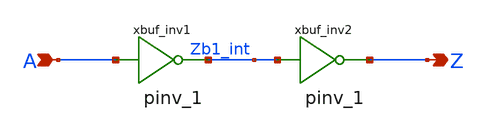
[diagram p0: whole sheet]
** sch_path: sram_2_64_scn4m/pdriver_5.sch
**.subckt pdriver_5 A Z
*.ipin A
*.opin Z
xbuf_inv1 A Zb1_int vdd gnd pinv_1
xbuf_inv2 Zb1_int Z vdd gnd pinv_1
**.ends

* expanding   symbol:  pinv_1.sym # of pins=2
** sym_path: sram_2_64_scn4m_lcc/pinv_1.sym
** sch_path: sram_2_64_scn4m_lcc/pinv_1.sch
.subckt pinv_1 A Z vdd gnd
*.ipin A
*.opin Z
Mpinv_nmos Z A gnd gnd n w=0.8u l=0.4u m=1
Mp_inv_pmos Z A vdd vdd p w=6.4u l=0.4u m=1
.ends

.end
